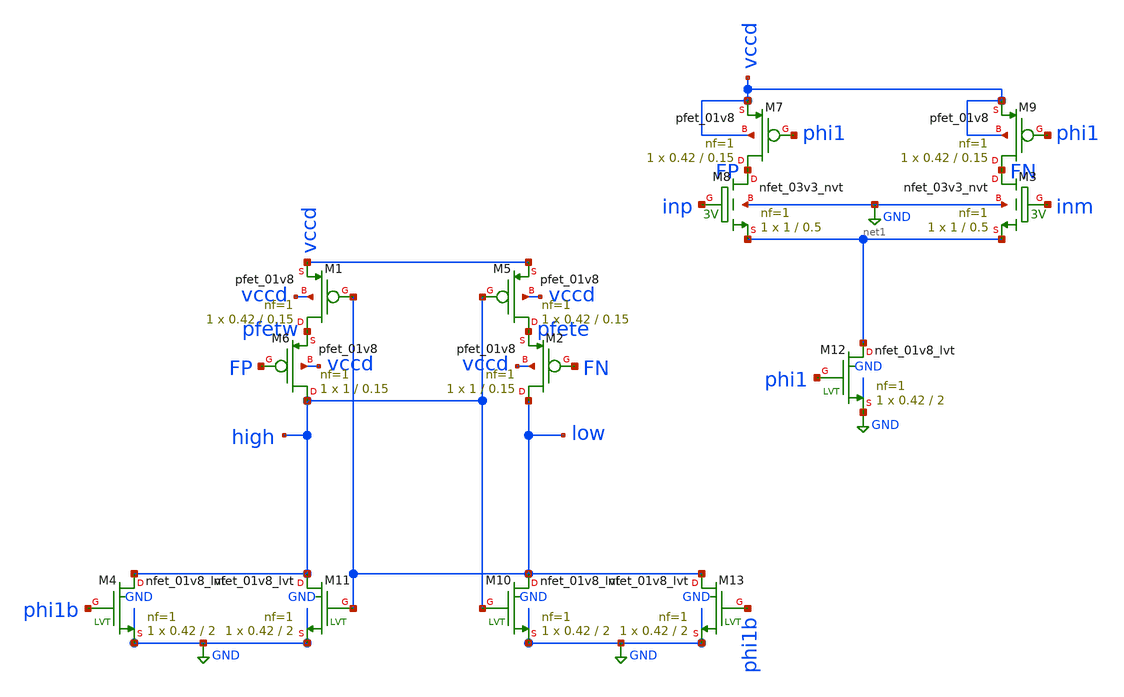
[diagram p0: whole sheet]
** sch_path: xschem/comparator_latest/comp_buf.sch
**.subckt comp_buf
XM6 high FP pfetw vccd sky130_fd_pr__pfet_01v8 L=0.15 W=1 nf=1 ad='int((nf+1)/2) * W/nf * 0.29' as='int((nf+2)/2) * W/nf * 0.29'
+ pd='2*int((nf+1)/2) * (W/nf + 0.29)' ps='2*int((nf+2)/2) * (W/nf + 0.29)' nrd='0.29 / W' nrs='0.29 / W'
+ sa=0 sb=0 sd=0 mult=1 m=1
XM2 low FN pfete vccd sky130_fd_pr__pfet_01v8 L=0.15 W=1 nf=1 ad='int((nf+1)/2) * W/nf * 0.29' as='int((nf+2)/2) * W/nf * 0.29'
+ pd='2*int((nf+1)/2) * (W/nf + 0.29)' ps='2*int((nf+2)/2) * (W/nf + 0.29)' nrd='0.29 / W' nrs='0.29 / W'
+ sa=0 sb=0 sd=0 mult=1 m=1
XM1 pfetw low vccd vccd sky130_fd_pr__pfet_01v8 L=0.15 W=0.42 nf=1 ad='int((nf+1)/2) * W/nf * 0.29' as='int((nf+2)/2) * W/nf * 0.29'
+ pd='2*int((nf+1)/2) * (W/nf + 0.29)' ps='2*int((nf+2)/2) * (W/nf + 0.29)' nrd='0.29 / W' nrs='0.29 / W'
+ sa=0 sb=0 sd=0 mult=1 m=1
XM5 pfete high vccd vccd sky130_fd_pr__pfet_01v8 L=0.15 W=0.42 nf=1 ad='int((nf+1)/2) * W/nf * 0.29'
+ as='int((nf+2)/2) * W/nf * 0.29' pd='2*int((nf+1)/2) * (W/nf + 0.29)' ps='2*int((nf+2)/2) * (W/nf + 0.29)'
+ nrd='0.29 / W' nrs='0.29 / W' sa=0 sb=0 sd=0 mult=1 m=1
XM4 high phi1b GND GND sky130_fd_pr__nfet_01v8_lvt L=2 W=0.42 nf=1 ad='int((nf+1)/2) * W/nf * 0.29' as='int((nf+2)/2) * W/nf * 0.29'
+ pd='2*int((nf+1)/2) * (W/nf + 0.29)' ps='2*int((nf+2)/2) * (W/nf + 0.29)' nrd='0.29 / W' nrs='0.29 / W'
+ sa=0 sb=0 sd=0 mult=1 m=1
XM10 low high GND GND sky130_fd_pr__nfet_01v8_lvt L=2 W=0.42 nf=1 ad='int((nf+1)/2) * W/nf * 0.29' as='int((nf+2)/2) * W/nf * 0.29'
+ pd='2*int((nf+1)/2) * (W/nf + 0.29)' ps='2*int((nf+2)/2) * (W/nf + 0.29)' nrd='0.29 / W' nrs='0.29 / W'
+ sa=0 sb=0 sd=0 mult=1 m=1
XM11 high low GND GND sky130_fd_pr__nfet_01v8_lvt L=2 W=0.42 nf=1 ad='int((nf+1)/2) * W/nf * 0.29' as='int((nf+2)/2) * W/nf * 0.29'
+ pd='2*int((nf+1)/2) * (W/nf + 0.29)' ps='2*int((nf+2)/2) * (W/nf + 0.29)' nrd='0.29 / W' nrs='0.29 / W'
+ sa=0 sb=0 sd=0 mult=1 m=1
XM13 low phi1b GND GND sky130_fd_pr__nfet_01v8_lvt L=2 W=0.42 nf=1 ad='int((nf+1)/2) * W/nf * 0.29' as='int((nf+2)/2) * W/nf * 0.29'
+ pd='2*int((nf+1)/2) * (W/nf + 0.29)' ps='2*int((nf+2)/2) * (W/nf + 0.29)' nrd='0.29 / W' nrs='0.29 / W'
+ sa=0 sb=0 sd=0 mult=1 m=1
XM7 FP phi1 vccd vccd sky130_fd_pr__pfet_01v8 L=0.15 W=0.42 nf=1 ad='int((nf+1)/2) * W/nf * 0.29' as='int((nf+2)/2) * W/nf * 0.29'
+ pd='2*int((nf+1)/2) * (W/nf + 0.29)' ps='2*int((nf+2)/2) * (W/nf + 0.29)' nrd='0.29 / W' nrs='0.29 / W'
+ sa=0 sb=0 sd=0 mult=1 m=1
XM9 FN phi1 vccd vccd sky130_fd_pr__pfet_01v8 L=0.15 W=0.42 nf=1 ad='int((nf+1)/2) * W/nf * 0.29' as='int((nf+2)/2) * W/nf * 0.29'
+ pd='2*int((nf+1)/2) * (W/nf + 0.29)' ps='2*int((nf+2)/2) * (W/nf + 0.29)' nrd='0.29 / W' nrs='0.29 / W'
+ sa=0 sb=0 sd=0 mult=1 m=1
XM3 FN inm net1 GND sky130_fd_pr__nfet_03v3_nvt L=0.5 W=1 nf=1 ad='int((nf+1)/2) * W/nf * 0.29' as='int((nf+2)/2) * W/nf * 0.29'
+ pd='2*int((nf+1)/2) * (W/nf + 0.29)' ps='2*int((nf+2)/2) * (W/nf + 0.29)' nrd='0.29 / W' nrs='0.29 / W'
+ sa=0 sb=0 sd=0 mult=1 m=1
XM8 FP inp net1 GND sky130_fd_pr__nfet_03v3_nvt L=0.5 W=1 nf=1 ad='int((nf+1)/2) * W/nf * 0.29' as='int((nf+2)/2) * W/nf * 0.29'
+ pd='2*int((nf+1)/2) * (W/nf + 0.29)' ps='2*int((nf+2)/2) * (W/nf + 0.29)' nrd='0.29 / W' nrs='0.29 / W'
+ sa=0 sb=0 sd=0 mult=1 m=1
XM12 net1 phi1 GND GND sky130_fd_pr__nfet_01v8_lvt L=2 W=0.42 nf=1 ad='int((nf+1)/2) * W/nf * 0.29' as='int((nf+2)/2) * W/nf * 0.29'
+ pd='2*int((nf+1)/2) * (W/nf + 0.29)' ps='2*int((nf+2)/2) * (W/nf + 0.29)' nrd='0.29 / W' nrs='0.29 / W'
+ sa=0 sb=0 sd=0 mult=1 m=1
**.ends
.GLOBAL GND
.end
